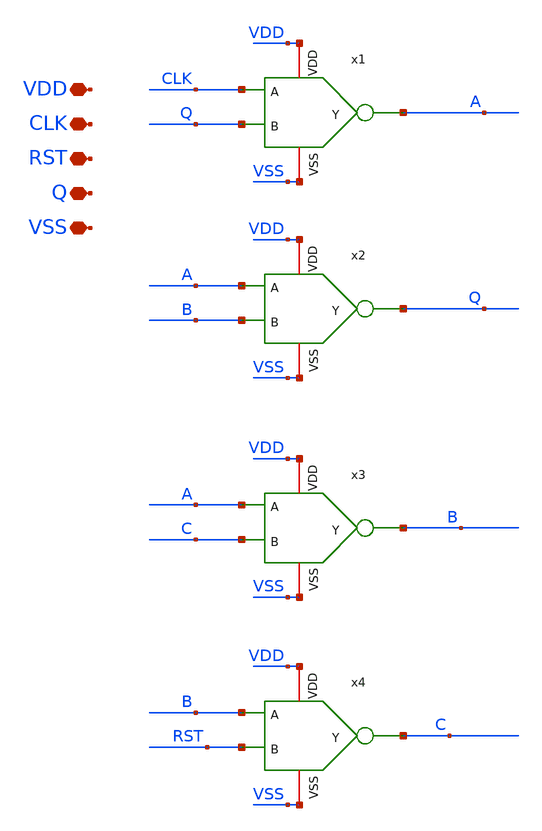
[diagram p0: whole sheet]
** sch_path: src/UN_PFD_GF180mcuD/UN_NDFF_GF180mcuD.sch
**.subckt UN_NDFF_GF180mcuD VDD CLK RST Q VSS
*.iopin VDD
*.iopin CLK
*.iopin RST
*.iopin Q
*.iopin VSS
x1 VDD CLK Q A VSS UN_NOR0_GF180mcuD
x2 VDD A B Q VSS UN_NOR0_GF180mcuD
x3 VDD A C B VSS UN_NOR0_GF180mcuD
x4 VDD B RST C VSS UN_NOR0_GF180mcuD
**.ends

* expanding   symbol:  /foss/designs/UN_BasicPLL_GF180mcuD/UN_PFD_GF180mcuD/UN_NOR0_GF180mcuD.sym #
*+ of pins=5
** sym_path: src/UN_PFD_GF180mcuD/UN_NOR0_GF180mcuD.sym
** sch_path: src/UN_PFD_GF180mcuD/UN_NOR0_GF180mcuD.sch
.subckt UN_NOR0_GF180mcuD VDD A B Y VSS
*.ipin A
*.ipin B
*.iopin VDD
*.iopin VSS
*.opin Y
XM1 Y A VSS VSS nfet_03v3 L=0.28u W=0.22u nf=1 ad='int((nf+1)/2) * W/nf * 0.18u' as='int((nf+2)/2) * W/nf * 0.18u'
+ pd='2*int((nf+1)/2) * (W/nf + 0.18u)' ps='2*int((nf+2)/2) * (W/nf + 0.18u)' nrd='0.18u / W' nrs='0.18u / W'
+ sa=0 sb=0 sd=0 m=1
XM2 Y B VSS VSS nfet_03v3 L=0.28u W=0.22u nf=1 ad='int((nf+1)/2) * W/nf * 0.18u' as='int((nf+2)/2) * W/nf * 0.18u'
+ pd='2*int((nf+1)/2) * (W/nf + 0.18u)' ps='2*int((nf+2)/2) * (W/nf + 0.18u)' nrd='0.18u / W' nrs='0.18u / W'
+ sa=0 sb=0 sd=0 m=1
XM3 Y B net1 VDD pfet_03v3 L=0.28u W=0.6u nf=1 ad='int((nf+1)/2) * W/nf * 0.18u' as='int((nf+2)/2) * W/nf * 0.18u'
+ pd='2*int((nf+1)/2) * (W/nf + 0.18u)' ps='2*int((nf+2)/2) * (W/nf + 0.18u)' nrd='0.18u / W' nrs='0.18u / W'
+ sa=0 sb=0 sd=0 m=1
XM4 net1 A VDD VDD pfet_03v3 L=0.28u W=0.6u nf=1 ad='int((nf+1)/2) * W/nf * 0.18u' as='int((nf+2)/2) * W/nf * 0.18u'
+ pd='2*int((nf+1)/2) * (W/nf + 0.18u)' ps='2*int((nf+2)/2) * (W/nf + 0.18u)' nrd='0.18u / W' nrs='0.18u / W'
+ sa=0 sb=0 sd=0 m=1
.ends

.end
